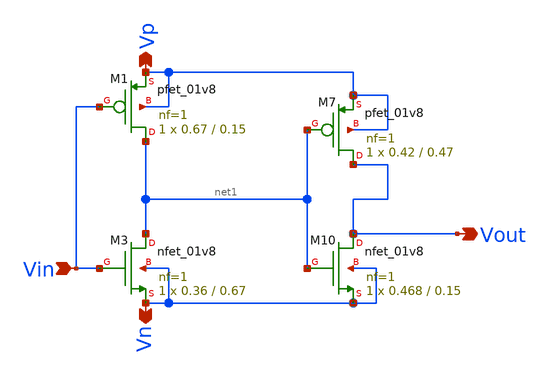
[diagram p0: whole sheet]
** sch_path: xschem/Vth_sch/Symbol/th08.sch
**.subckt th08 Vn Vp Vin Vout
*.opin Vn
*.opin Vp
*.ipin Vin
*.opin Vout
XM7 Vout net1 Vp Vp sky130_fd_pr__pfet_01v8 L=0.47 W=0.42 nf=1 ad='int((nf+1)/2) * W/nf * 0.29' as='int((nf+2)/2) * W/nf * 0.29'
+ pd='2*int((nf+1)/2) * (W/nf + 0.29)' ps='2*int((nf+2)/2) * (W/nf + 0.29)' nrd='0.29 / W' nrs='0.29 / W'
+ sa=0 sb=0 sd=0 mult=1 m=1
XM10 Vout net1 Vn Vn sky130_fd_pr__nfet_01v8 L=0.15 W=0.468 nf=1 ad='int((nf+1)/2) * W/nf * 0.29' as='int((nf+2)/2) * W/nf * 0.29'
+ pd='2*int((nf+1)/2) * (W/nf + 0.29)' ps='2*int((nf+2)/2) * (W/nf + 0.29)' nrd='0.29 / W' nrs='0.29 / W'
+ sa=0 sb=0 sd=0 mult=1 m=1
XM1 net1 Vin Vp Vp sky130_fd_pr__pfet_01v8 L=0.15 W=0.67 nf=1 ad='int((nf+1)/2) * W/nf * 0.29' as='int((nf+2)/2) * W/nf * 0.29'
+ pd='2*int((nf+1)/2) * (W/nf + 0.29)' ps='2*int((nf+2)/2) * (W/nf + 0.29)' nrd='0.29 / W' nrs='0.29 / W'
+ sa=0 sb=0 sd=0 mult=1 m=1
XM3 net1 Vin Vn Vn sky130_fd_pr__nfet_01v8 L=0.67 W=0.36 nf=1 ad='int((nf+1)/2) * W/nf * 0.29' as='int((nf+2)/2) * W/nf * 0.29'
+ pd='2*int((nf+1)/2) * (W/nf + 0.29)' ps='2*int((nf+2)/2) * (W/nf + 0.29)' nrd='0.29 / W' nrs='0.29 / W'
+ sa=0 sb=0 sd=0 mult=1 m=1
**.ends
.end
